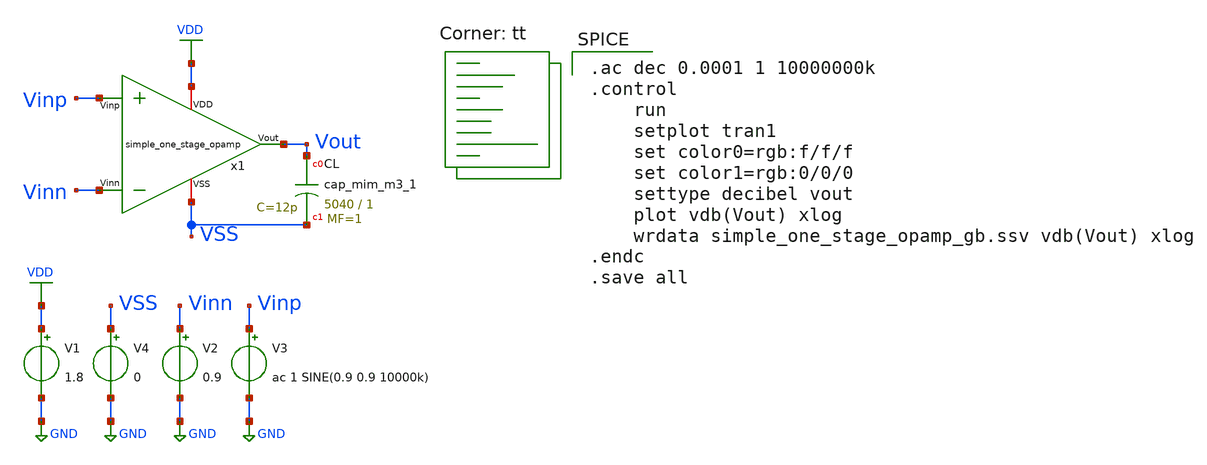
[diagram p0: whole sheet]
** sch_path: opamp_design/simple_one_stage_opamp/simple_one_stage_opamp_gb.sch
**.subckt simple_one_stage_opamp_gb
V1 VDD GND 1.8
V2 Vinn GND 0.9
V3 Vinp GND ac 1 SINE(0.9 0.9 10000k)
V4 VSS GND 0
x1 VDD Vout Vinp Vinn VSS simple_one_stage_opamp
XCL Vout VSS sky130_fd_pr__cap_mim_m3_1 W=5040 L=1 MF=1 m=1
**** begin user architecture code

.ac dec 0.0001 1 10000000k
.control
	run
	setplot tran1
	set color0=rgb:f/f/f
	set color1=rgb:0/0/0
	settype decibel vout
	plot vdb(Vout) xlog
	wrdata simple_one_stage_opamp_gb.ssv vdb(Vout) xlog
.endc
.save all


.lib $::SKYWATER_MODELS/sky130.lib.spice tt
**** end user architecture code
**.ends

* expanding   symbol:
*+  /home/ricardo/RATT_repos/Proyectos_xschem/opamp_design/simple_one_stage_opamp/simple_one_stage_opamp.sym # of pins=5
** sym_path: opamp_design/simple_one_stage_opamp/simple_one_stage_opamp.sym
** sch_path: opamp_design/simple_one_stage_opamp/simple_one_stage_opamp.sch
.subckt simple_one_stage_opamp VDD Vout Vinp Vinn VSS
*.iopin VSS
*.iopin VDD
*.ipin Vinp
*.ipin Vinn
*.opin Vout
XM1 net2 Vinp net1 VSS sky130_fd_pr__nfet_01v8 L=0.15 W=15.648 nf=1 ad='int((nf+1)/2) * W/nf * 0.29'
+ as='int((nf+2)/2) * W/nf * 0.29' pd='2*int((nf+1)/2) * (W/nf + 0.29)' ps='2*int((nf+2)/2) * (W/nf + 0.29)'
+ nrd='0.29 / W' nrs='0.29 / W' sa=0 sb=0 sd=0 mult=1 m=1
XM4 net2 net2 VDD VDD sky130_fd_pr__pfet_01v8 L=0.15 W=0.449 nf=1 ad='int((nf+1)/2) * W/nf * 0.29' as='int((nf+2)/2) * W/nf * 0.29'
+ pd='2*int((nf+1)/2) * (W/nf + 0.29)' ps='2*int((nf+2)/2) * (W/nf + 0.29)' nrd='0.29 / W' nrs='0.29 / W'
+ sa=0 sb=0 sd=0 mult=1 m=1
XM2 Vout Vinn net1 VSS sky130_fd_pr__nfet_01v8 L=0.15 W=15.648 nf=1 ad='int((nf+1)/2) * W/nf * 0.29'
+ as='int((nf+2)/2) * W/nf * 0.29' pd='2*int((nf+1)/2) * (W/nf + 0.29)' ps='2*int((nf+2)/2) * (W/nf + 0.29)'
+ nrd='0.29 / W' nrs='0.29 / W' sa=0 sb=0 sd=0 mult=1 m=1
XM3 Vout net2 VDD VDD sky130_fd_pr__pfet_01v8 L=0.15 W=0.449 nf=1 ad='int((nf+1)/2) * W/nf * 0.29' as='int((nf+2)/2) * W/nf * 0.29'
+ pd='2*int((nf+1)/2) * (W/nf + 0.29)' ps='2*int((nf+2)/2) * (W/nf + 0.29)' nrd='0.29 / W' nrs='0.29 / W'
+ sa=0 sb=0 sd=0 mult=1 m=1
XM5 net1 net3 VSS VSS sky130_fd_pr__nfet_01v8 L=0.15 W=5.193 nf=1 ad='int((nf+1)/2) * W/nf * 0.29' as='int((nf+2)/2) * W/nf * 0.29'
+ pd='2*int((nf+1)/2) * (W/nf + 0.29)' ps='2*int((nf+2)/2) * (W/nf + 0.29)' nrd='0.29 / W' nrs='0.29 / W'
+ sa=0 sb=0 sd=0 mult=1 m=1
XM6 net3 net3 VSS VSS sky130_fd_pr__nfet_01v8 L=0.15 W=5.193 nf=1 ad='int((nf+1)/2) * W/nf * 0.29' as='int((nf+2)/2) * W/nf * 0.29'
+ pd='2*int((nf+1)/2) * (W/nf + 0.29)' ps='2*int((nf+2)/2) * (W/nf + 0.29)' nrd='0.29 / W' nrs='0.29 / W'
+ sa=0 sb=0 sd=0 mult=1 m=1
I0 VDD net3 48u
.ends

.GLOBAL VDD
.GLOBAL GND
.end
